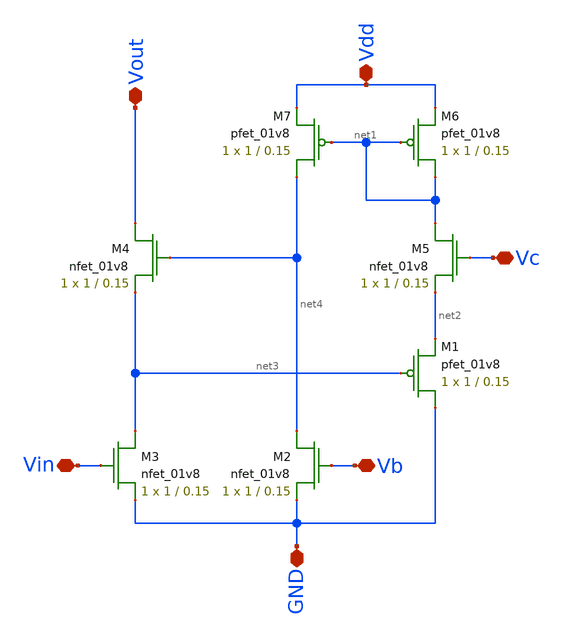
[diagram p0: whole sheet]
** sch_path: triode.sch
**.subckt triode Vout Vc Vb Vin GND Vdd
*.iopin Vout
*.iopin Vc
*.iopin Vb
*.iopin Vin
*.iopin GND
*.iopin Vdd
XM7 net4 net1 Vdd VDD sky130_fd_pr__pfet_01v8 L=0.15 W=1 nf=1 ad='int((nf+1)/2) * W/nf * 0.29' as='int((nf+2)/2) * W/nf * 0.29'
+ pd='2*int((nf+1)/2) * (W/nf + 0.29)' ps='2*int((nf+2)/2) * (W/nf + 0.29)' nrd='0.29 / W' nrs='0.29 / W'
+ sa=0 sb=0 sd=0 mult=1 m=1
XM6 net1 net1 Vdd VDD sky130_fd_pr__pfet_01v8 L=0.15 W=1 nf=1 ad='int((nf+1)/2) * W/nf * 0.29' as='int((nf+2)/2) * W/nf * 0.29'
+ pd='2*int((nf+1)/2) * (W/nf + 0.29)' ps='2*int((nf+2)/2) * (W/nf + 0.29)' nrd='0.29 / W' nrs='0.29 / W'
+ sa=0 sb=0 sd=0 mult=1 m=1
XM5 net1 Vc net2 GND sky130_fd_pr__nfet_01v8 L=0.15 W=1 nf=1 ad='int((nf+1)/2) * W/nf * 0.29' as='int((nf+2)/2) * W/nf * 0.29'
+ pd='2*int((nf+1)/2) * (W/nf + 0.29)' ps='2*int((nf+2)/2) * (W/nf + 0.29)' nrd='0.29 / W' nrs='0.29 / W'
+ sa=0 sb=0 sd=0 mult=1 m=1
XM1 GND net3 net2 VDD sky130_fd_pr__pfet_01v8 L=0.15 W=1 nf=1 ad='int((nf+1)/2) * W/nf * 0.29' as='int((nf+2)/2) * W/nf * 0.29'
+ pd='2*int((nf+1)/2) * (W/nf + 0.29)' ps='2*int((nf+2)/2) * (W/nf + 0.29)' nrd='0.29 / W' nrs='0.29 / W'
+ sa=0 sb=0 sd=0 mult=1 m=1
XM2 net4 Vb GND GND sky130_fd_pr__nfet_01v8 L=0.15 W=1 nf=1 ad='int((nf+1)/2) * W/nf * 0.29' as='int((nf+2)/2) * W/nf * 0.29'
+ pd='2*int((nf+1)/2) * (W/nf + 0.29)' ps='2*int((nf+2)/2) * (W/nf + 0.29)' nrd='0.29 / W' nrs='0.29 / W'
+ sa=0 sb=0 sd=0 mult=1 m=1
XM3 net3 Vin GND GND sky130_fd_pr__nfet_01v8 L=0.15 W=1 nf=1 ad='int((nf+1)/2) * W/nf * 0.29' as='int((nf+2)/2) * W/nf * 0.29'
+ pd='2*int((nf+1)/2) * (W/nf + 0.29)' ps='2*int((nf+2)/2) * (W/nf + 0.29)' nrd='0.29 / W' nrs='0.29 / W'
+ sa=0 sb=0 sd=0 mult=1 m=1
XM4 Vout net4 net3 GND sky130_fd_pr__nfet_01v8 L=0.15 W=1 nf=1 ad='int((nf+1)/2) * W/nf * 0.29' as='int((nf+2)/2) * W/nf * 0.29'
+ pd='2*int((nf+1)/2) * (W/nf + 0.29)' ps='2*int((nf+2)/2) * (W/nf + 0.29)' nrd='0.29 / W' nrs='0.29 / W'
+ sa=0 sb=0 sd=0 mult=1 m=1
**.ends
.end
